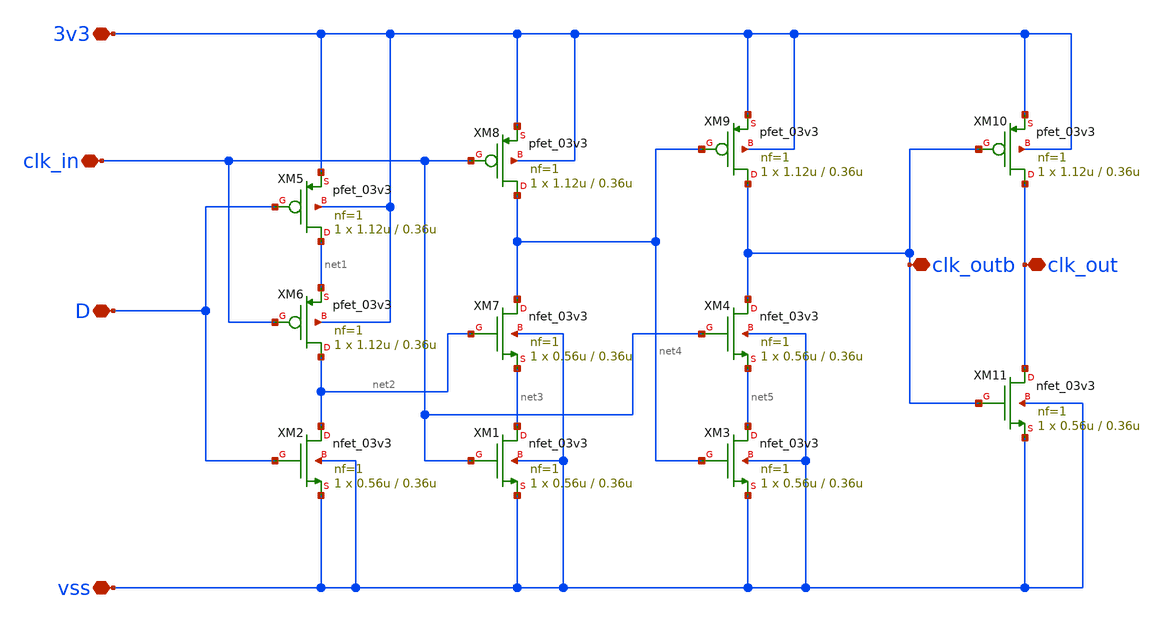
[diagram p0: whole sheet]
** sch_path: PLL/analog/schematics/Division_flipflop.sch
**.subckt Division_flipflop 3v3 vss clk_outb D clk_in clk_out
*.iopin 3v3
*.iopin vss
*.iopin clk_outb
*.iopin D
*.iopin clk_in
*.iopin clk_out
XM1 net3 clk_in vss vss nfet_03v3 L=0.36u W=0.56u nf=1 ad='int((nf+1)/2) * W/nf * 0.18u' as='int((nf+2)/2) * W/nf * 0.18u'
+ pd='2*int((nf+1)/2) * (W/nf + 0.18u)' ps='2*int((nf+2)/2) * (W/nf + 0.18u)' nrd='0.18u / W' nrs='0.18u / W'
+ sa=0 sb=0 sd=0 m=1
XM2 net2 D vss vss nfet_03v3 L=0.36u W=0.56u nf=1 ad='int((nf+1)/2) * W/nf * 0.18u' as='int((nf+2)/2) * W/nf * 0.18u'
+ pd='2*int((nf+1)/2) * (W/nf + 0.18u)' ps='2*int((nf+2)/2) * (W/nf + 0.18u)' nrd='0.18u / W' nrs='0.18u / W'
+ sa=0 sb=0 sd=0 m=1
XM3 net5 net4 vss vss nfet_03v3 L=0.36u W=0.56u nf=1 ad='int((nf+1)/2) * W/nf * 0.18u' as='int((nf+2)/2) * W/nf * 0.18u'
+ pd='2*int((nf+1)/2) * (W/nf + 0.18u)' ps='2*int((nf+2)/2) * (W/nf + 0.18u)' nrd='0.18u / W' nrs='0.18u / W'
+ sa=0 sb=0 sd=0 m=1
XM4 clk_outb clk_in net5 vss nfet_03v3 L=0.36u W=0.56u nf=1 ad='int((nf+1)/2) * W/nf * 0.18u' as='int((nf+2)/2) * W/nf * 0.18u'
+ pd='2*int((nf+1)/2) * (W/nf + 0.18u)' ps='2*int((nf+2)/2) * (W/nf + 0.18u)' nrd='0.18u / W' nrs='0.18u / W'
+ sa=0 sb=0 sd=0 m=1
XM5 net1 D 3v3 3v3 pfet_03v3 L=0.36u W=1.12u nf=1 ad='int((nf+1)/2) * W/nf * 0.18u' as='int((nf+2)/2) * W/nf * 0.18u'
+ pd='2*int((nf+1)/2) * (W/nf + 0.18u)' ps='2*int((nf+2)/2) * (W/nf + 0.18u)' nrd='0.18u / W' nrs='0.18u / W'
+ sa=0 sb=0 sd=0 m=1
XM6 net2 clk_in net1 3v3 pfet_03v3 L=0.36u W=1.12u nf=1 ad='int((nf+1)/2) * W/nf * 0.18u' as='int((nf+2)/2) * W/nf * 0.18u'
+ pd='2*int((nf+1)/2) * (W/nf + 0.18u)' ps='2*int((nf+2)/2) * (W/nf + 0.18u)' nrd='0.18u / W' nrs='0.18u / W'
+ sa=0 sb=0 sd=0 m=1
XM8 net4 clk_in 3v3 3v3 pfet_03v3 L=0.36u W=1.12u nf=1 ad='int((nf+1)/2) * W/nf * 0.18u' as='int((nf+2)/2) * W/nf * 0.18u'
+ pd='2*int((nf+1)/2) * (W/nf + 0.18u)' ps='2*int((nf+2)/2) * (W/nf + 0.18u)' nrd='0.18u / W' nrs='0.18u / W'
+ sa=0 sb=0 sd=0 m=1
XM9 clk_outb net4 3v3 3v3 pfet_03v3 L=0.36u W=1.12u nf=1 ad='int((nf+1)/2) * W/nf * 0.18u' as='int((nf+2)/2) * W/nf * 0.18u'
+ pd='2*int((nf+1)/2) * (W/nf + 0.18u)' ps='2*int((nf+2)/2) * (W/nf + 0.18u)' nrd='0.18u / W' nrs='0.18u / W'
+ sa=0 sb=0 sd=0 m=1
XM7 net4 net2 net3 vss nfet_03v3 L=0.36u W=0.56u nf=1 ad='int((nf+1)/2) * W/nf * 0.18u' as='int((nf+2)/2) * W/nf * 0.18u'
+ pd='2*int((nf+1)/2) * (W/nf + 0.18u)' ps='2*int((nf+2)/2) * (W/nf + 0.18u)' nrd='0.18u / W' nrs='0.18u / W'
+ sa=0 sb=0 sd=0 m=1
XM10 clk_out clk_outb 3v3 3v3 pfet_03v3 L=0.36u W=1.12u nf=1 ad='int((nf+1)/2) * W/nf * 0.18u' as='int((nf+2)/2) * W/nf * 0.18u'
+ pd='2*int((nf+1)/2) * (W/nf + 0.18u)' ps='2*int((nf+2)/2) * (W/nf + 0.18u)' nrd='0.18u / W' nrs='0.18u / W'
+ sa=0 sb=0 sd=0 m=1
XM11 clk_out clk_outb vss vss nfet_03v3 L=0.36u W=0.56u nf=1 ad='int((nf+1)/2) * W/nf * 0.18u' as='int((nf+2)/2) * W/nf * 0.18u'
+ pd='2*int((nf+1)/2) * (W/nf + 0.18u)' ps='2*int((nf+2)/2) * (W/nf + 0.18u)' nrd='0.18u / W' nrs='0.18u / W'
+ sa=0 sb=0 sd=0 m=1
**.ends
.end
